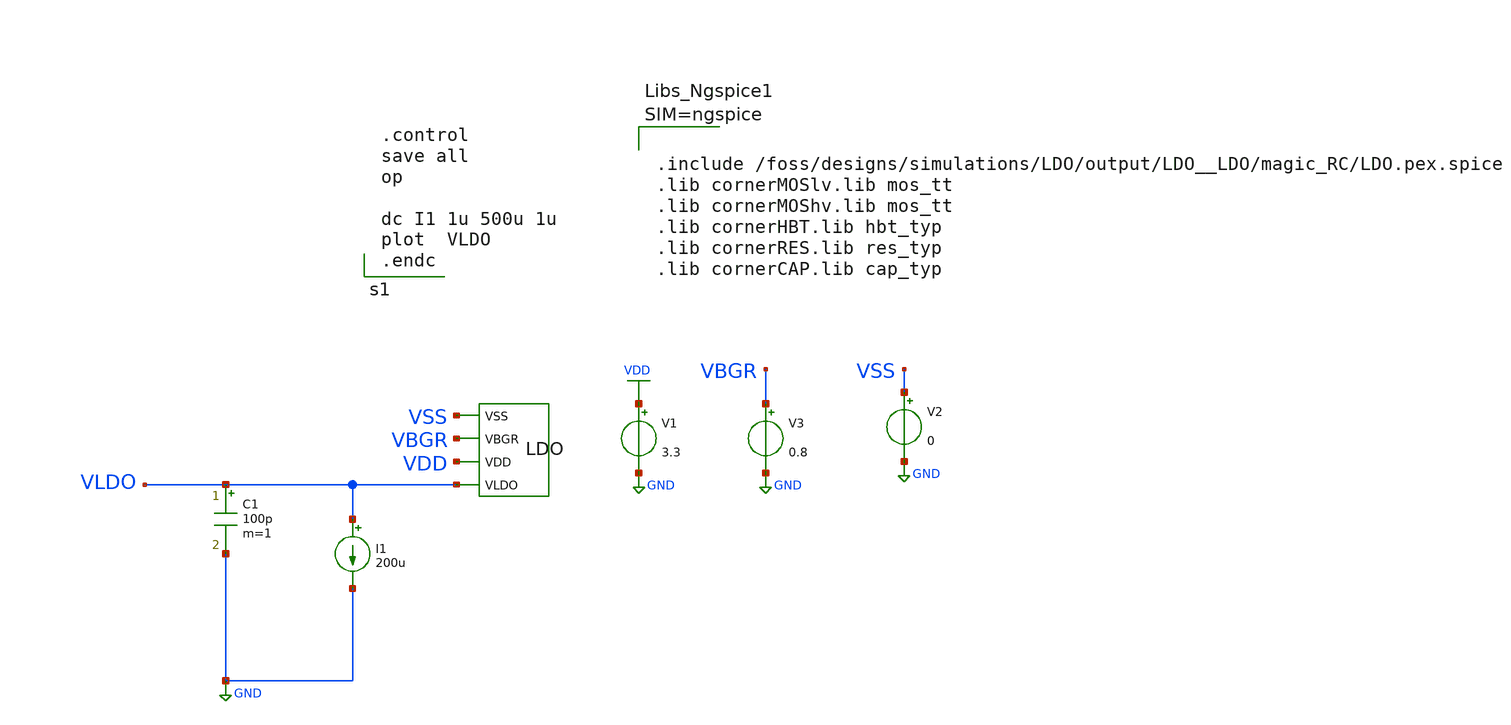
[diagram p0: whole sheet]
** sch_path: dependencies/LDO/LDO-main/testbenches/line-regulation/ldo_post_layout_sim_dc_LoadRegulation.sch
**.subckt ldo_post_layout_sim_dc_LoadRegulation
V1 VDD GND 3.3
V3 VBGR GND 0.8
V2 VSS GND 0
X1 VSS VBGR VDD VLDO LDO
C1 VLDO GND 100p m=1
I1 VLDO GND 200u
**** begin user architecture code



.include /foss/designs/simulations/LDO/output/LDO__LDO/magic_RC/LDO.pex.spice
.lib cornerMOSlv.lib mos_tt
.lib cornerMOShv.lib mos_tt
.lib cornerHBT.lib hbt_typ
.lib cornerRES.lib res_typ
.lib cornerCAP.lib cap_typ





.control
save all
op

dc I1 1u 500u 1u
plot  VLDO
.endc

**** end user architecture code
**.ends
.GLOBAL GND
.GLOBAL VDD
.end
